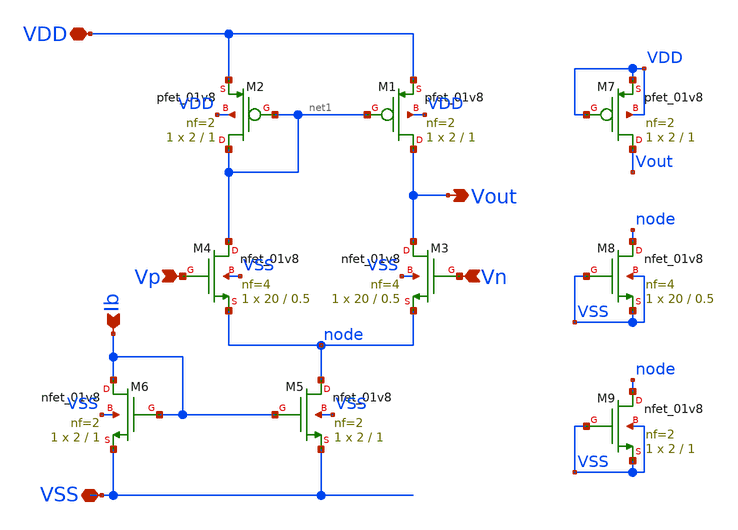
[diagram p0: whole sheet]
** sch_path: examples/sky130_cace_ip__ota5t/xschem/sky130_cace_ip__ota5t.sch
**.subckt sky130_cace_ip__ota5t Vp Vn Vout VDD VSS Ib
*.ipin Vp
*.ipin Vn
*.opin Vout
*.iopin VDD
*.iopin VSS
*.ipin Ib
XM4 net1 Vp node VSS sky130_fd_pr__nfet_01v8 L=0.5 W=20 nf=4 ad='int((nf+1)/2) * W/nf * 0.29' as='int((nf+2)/2) * W/nf * 0.29'
+ pd='2*int((nf+1)/2) * (W/nf + 0.29)' ps='2*int((nf+2)/2) * (W/nf + 0.29)' nrd='0.29 / W' nrs='0.29 / W'
+ sa=0 sb=0 sd=0 mult=1 m=1
XM1 Vout net1 VDD VDD sky130_fd_pr__pfet_01v8 L=1 W=2 nf=2 ad='int((nf+1)/2) * W/nf * 0.29' as='int((nf+2)/2) * W/nf * 0.29'
+ pd='2*int((nf+1)/2) * (W/nf + 0.29)' ps='2*int((nf+2)/2) * (W/nf + 0.29)' nrd='0.29 / W' nrs='0.29 / W'
+ sa=0 sb=0 sd=0 mult=1 m=1
XM2 net1 net1 VDD VDD sky130_fd_pr__pfet_01v8 L=1 W=2 nf=2 ad='int((nf+1)/2) * W/nf * 0.29' as='int((nf+2)/2) * W/nf * 0.29'
+ pd='2*int((nf+1)/2) * (W/nf + 0.29)' ps='2*int((nf+2)/2) * (W/nf + 0.29)' nrd='0.29 / W' nrs='0.29 / W'
+ sa=0 sb=0 sd=0 mult=1 m=1
XM3 Vout Vn node VSS sky130_fd_pr__nfet_01v8 L=0.5 W=20 nf=4 ad='int((nf+1)/2) * W/nf * 0.29' as='int((nf+2)/2) * W/nf * 0.29'
+ pd='2*int((nf+1)/2) * (W/nf + 0.29)' ps='2*int((nf+2)/2) * (W/nf + 0.29)' nrd='0.29 / W' nrs='0.29 / W'
+ sa=0 sb=0 sd=0 mult=1 m=1
XM5 node Ib VSS VSS sky130_fd_pr__nfet_01v8 L=1 W=2 nf=2 ad='int((nf+1)/2) * W/nf * 0.29' as='int((nf+2)/2) * W/nf * 0.29'
+ pd='2*int((nf+1)/2) * (W/nf + 0.29)' ps='2*int((nf+2)/2) * (W/nf + 0.29)' nrd='0.29 / W' nrs='0.29 / W'
+ sa=0 sb=0 sd=0 mult=1 m=1
XM6 Ib Ib VSS VSS sky130_fd_pr__nfet_01v8 L=1 W=2 nf=2 ad='int((nf+1)/2) * W/nf * 0.29' as='int((nf+2)/2) * W/nf * 0.29'
+ pd='2*int((nf+1)/2) * (W/nf + 0.29)' ps='2*int((nf+2)/2) * (W/nf + 0.29)' nrd='0.29 / W' nrs='0.29 / W'
+ sa=0 sb=0 sd=0 mult=1 m=1
XM7 Vout VDD VDD VDD sky130_fd_pr__pfet_01v8 L=1 W=2 nf=2 ad='int((nf+1)/2) * W/nf * 0.29' as='int((nf+2)/2) * W/nf * 0.29'
+ pd='2*int((nf+1)/2) * (W/nf + 0.29)' ps='2*int((nf+2)/2) * (W/nf + 0.29)' nrd='0.29 / W' nrs='0.29 / W'
+ sa=0 sb=0 sd=0 mult=1 m=1
XM8 node VSS VSS VSS sky130_fd_pr__nfet_01v8 L=0.5 W=20 nf=4 ad='int((nf+1)/2) * W/nf * 0.29' as='int((nf+2)/2) * W/nf * 0.29'
+ pd='2*int((nf+1)/2) * (W/nf + 0.29)' ps='2*int((nf+2)/2) * (W/nf + 0.29)' nrd='0.29 / W' nrs='0.29 / W'
+ sa=0 sb=0 sd=0 mult=1 m=1
XM9 node VSS VSS VSS sky130_fd_pr__nfet_01v8 L=1 W=2 nf=2 ad='int((nf+1)/2) * W/nf * 0.29' as='int((nf+2)/2) * W/nf * 0.29'
+ pd='2*int((nf+1)/2) * (W/nf + 0.29)' ps='2*int((nf+2)/2) * (W/nf + 0.29)' nrd='0.29 / W' nrs='0.29 / W'
+ sa=0 sb=0 sd=0 mult=1 m=1
**.ends
.end
